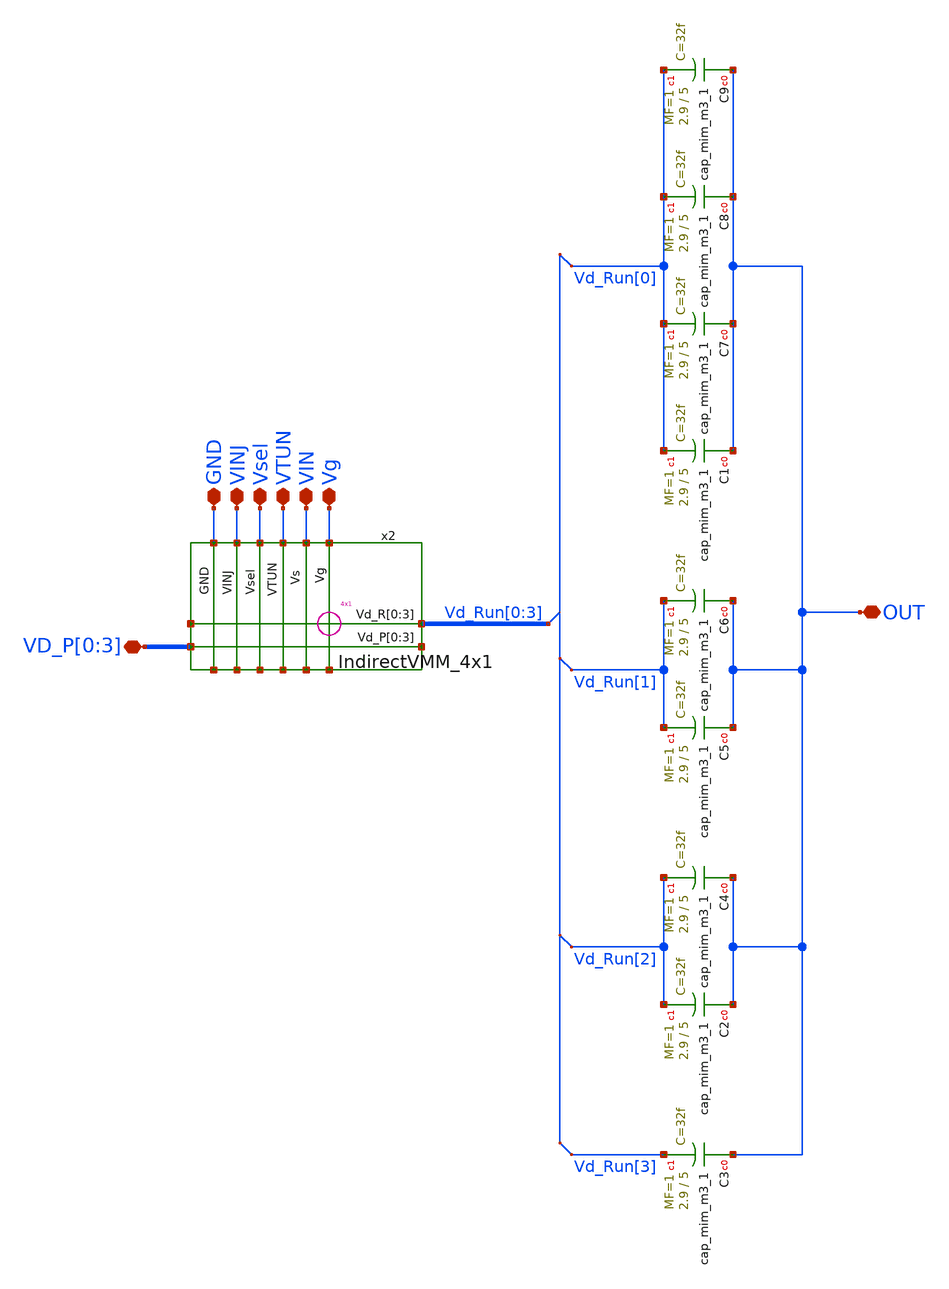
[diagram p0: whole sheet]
** sch_path: sky130_cells/Cap_Bank/Cap_Bank.sch
**.subckt Cap_Bank VTUN GND VINJ VIN Vsel Vg VD_P[0],VD_P[1],VD_P[2],VD_P[3] OUT
*.iopin VTUN
*.iopin GND
*.iopin VINJ
*.iopin VIN
*.iopin Vsel
*.iopin Vg
*.iopin VD_P[0],VD_P[1],VD_P[2],VD_P[3]
*.iopin OUT
x2 VD_P[0] VD_P[1] VD_P[2] VD_P[3] Vd_Run[0] Vd_Run[1] Vd_Run[2] Vd_Run[3] Vg VIN VTUN Vsel VINJ GND
+ IndirectVMM_4x1
XC3 OUT Vd_Run[3] sky130_fd_pr__cap_mim_m3_1 W=2.9 L=5 MF=1 m=1
XC2 OUT Vd_Run[2] sky130_fd_pr__cap_mim_m3_1 W=2.9 L=5 MF=1 m=1
* tap: #net1 --> Vd_Run[0]
* tap: #net1 --> Vd_Run[1]
* tap: #net1 --> Vd_Run[2]
* tap: #net1 --> Vd_Run[3]
XC4 OUT Vd_Run[2] sky130_fd_pr__cap_mim_m3_1 W=2.9 L=5 MF=1 m=1
XC5 OUT Vd_Run[1] sky130_fd_pr__cap_mim_m3_1 W=2.9 L=5 MF=1 m=1
XC6 OUT Vd_Run[1] sky130_fd_pr__cap_mim_m3_1 W=2.9 L=5 MF=1 m=1
XC1 OUT Vd_Run[0] sky130_fd_pr__cap_mim_m3_1 W=2.9 L=5 MF=1 m=1
XC7 OUT Vd_Run[0] sky130_fd_pr__cap_mim_m3_1 W=2.9 L=5 MF=1 m=1
XC8 OUT Vd_Run[0] sky130_fd_pr__cap_mim_m3_1 W=2.9 L=5 MF=1 m=1
XC9 OUT Vd_Run[0] sky130_fd_pr__cap_mim_m3_1 W=2.9 L=5 MF=1 m=1
**.ends

* expanding   symbol:  sky130_cells/IndirectVMM_4x1/IndirectVMM_4x1.sym # of pins=16
** sym_path: sky130_cells/IndirectVMM_4x1/IndirectVMM_4x1.sym
** sch_path: sky130_cells/IndirectVMM_4x1/IndirectVMM_4x1.sch
.subckt IndirectVMM_4x1 Vd_P[0] Vd_P[1] Vd_P[2] Vd_P[3] Vd_R[0] Vd_R[1] Vd_R[2] Vd_R[3] Vg Vs VTUN
+ Vsel VINJ GND
*.iopin Vd_R[0],Vd_R[1],Vd_R[2],Vd_R[3]
*.iopin Vd_P[0],Vd_P[1],Vd_P[2],Vd_P[3]
*.iopin Vg
*.iopin VTUN
*.iopin Vsel
*.iopin GND
*.iopin VINJ
*.iopin Vs
x5[0] Vs Vg Vsel VTUN Vd_R[0] Vd_P[0] VINJ GND FG_Indirect
x5[1] Vs Vg Vsel VTUN Vd_R[1] Vd_P[1] VINJ GND FG_Indirect
x5[2] Vs Vg Vsel VTUN Vd_R[2] Vd_P[2] VINJ GND FG_Indirect
x5[3] Vs Vg Vsel VTUN Vd_R[3] Vd_P[3] VINJ GND FG_Indirect
.ends


* expanding   symbol:  sky130_cells/Floating_Gates/Indirect/FG_Indirect.sym # of pins=16
** sym_path: sky130_cells/Floating_Gates/Indirect/FG_Indirect.sym
** sch_path: sky130_cells/Floating_Gates/Indirect/FG_Indirect.sch
.subckt FG_Indirect Vs Vg Vsel VTUN Vd_R Vd_P VINJ GND
*.iopin VINJ
*.iopin Vsel
*.iopin Vg
*.iopin Vs
*.iopin Vd_R
*.iopin Vd_P
*.iopin VTUN
*.iopin GND
XM1 Vd_R Vfg Vs VINJ sky130_fd_pr__pfet_g5v0d10v5 L=0.5 W=0.42 nf=1 ad='int((nf+1)/2) * W/nf * 0.29'
+ as='int((nf+2)/2) * W/nf * 0.29' pd='2*int((nf+1)/2) * (W/nf + 0.29)' ps='2*int((nf+2)/2) * (W/nf + 0.29)'
+ nrd='0.29 / W' nrs='0.29 / W' sa=0 sb=0 sd=0 mult=1 m=1
XM2 net1 Vsel VINJ VINJ sky130_fd_pr__pfet_g5v0d10v5 L=0.5 W=0.42 nf=1 ad='int((nf+1)/2) * W/nf * 0.29'
+ as='int((nf+2)/2) * W/nf * 0.29' pd='2*int((nf+1)/2) * (W/nf + 0.29)' ps='2*int((nf+2)/2) * (W/nf + 0.29)'
+ nrd='0.29 / W' nrs='0.29 / W' sa=0 sb=0 sd=0 mult=1 m=1
XM3 Vd_P Vfg net1 VINJ sky130_fd_pr__pfet_g5v0d10v5 L=0.5 W=0.42 nf=1 ad='int((nf+1)/2) * W/nf * 0.29'
+ as='int((nf+2)/2) * W/nf * 0.29' pd='2*int((nf+1)/2) * (W/nf + 0.29)' ps='2*int((nf+2)/2) * (W/nf + 0.29)'
+ nrd='0.29 / W' nrs='0.29 / W' sa=0 sb=0 sd=0 mult=1 m=1
XC1 Vfg VTUN GND sky130_fd_pr__cap_var_hvt W=0.29 L=0.5 VM=1 m=1
XC2 Vfg Vg GND sky130_fd_pr__cap_var_hvt W=0.54 L=0.65 VM=1 m=1
.ends

.end
